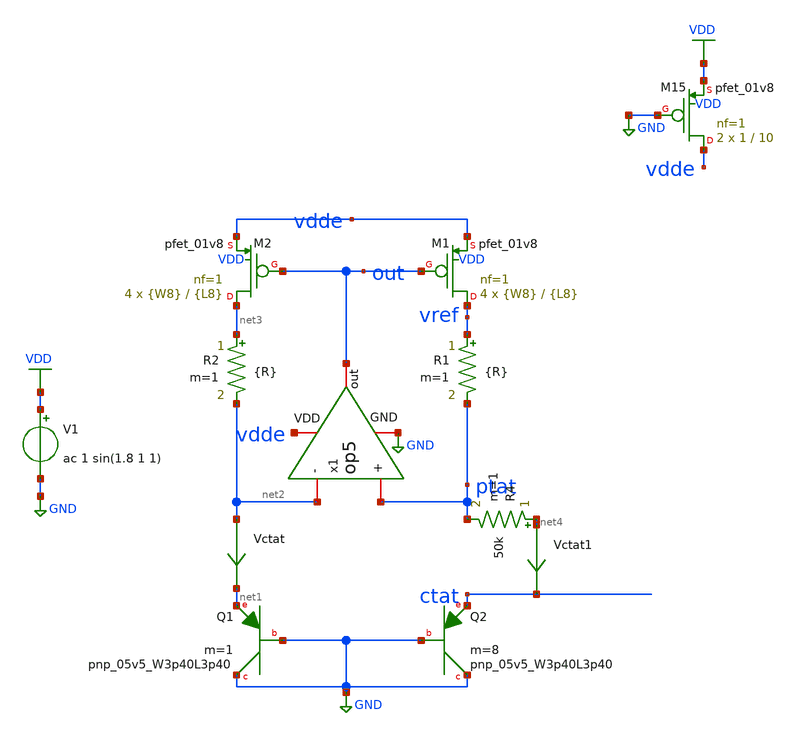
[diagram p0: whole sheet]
** sch_path: xschem/bgr_op5_ideal.sch
**.subckt bgr_op5_ideal
XQ1 GND GND net1 sky130_fd_pr__pnp_05v5_W3p40L3p40 m=1
XQ2 GND GND ctat sky130_fd_pr__pnp_05v5_W3p40L3p40 m=8
Vctat net2 net1 0
.save i(vctat)
V1 VDD GND ac 1 sin(1.8 1 1)
XM1 vref out vdde VDD sky130_fd_pr__pfet_01v8 L={L8} W={W8} nf=1 ad='int((nf+1)/2) * W/nf * 0.29' as='int((nf+2)/2) * W/nf * 0.29'
+ pd='2*int((nf+1)/2) * (W/nf + 0.29)' ps='2*int((nf+2)/2) * (W/nf + 0.29)' nrd='0.29 / W' nrs='0.29 / W'
+ sa=0 sb=0 sd=0 mult=4 m=4
XM2 net3 out vdde VDD sky130_fd_pr__pfet_01v8 L={L8} W={W8} nf=1 ad='int((nf+1)/2) * W/nf * 0.29' as='int((nf+2)/2) * W/nf * 0.29'
+ pd='2*int((nf+1)/2) * (W/nf + 0.29)' ps='2*int((nf+2)/2) * (W/nf + 0.29)' nrd='0.29 / W' nrs='0.29 / W'
+ sa=0 sb=0 sd=0 mult=4 m=4
x1 vdde out net2 ptat GND op5
XM15 vdde GND VDD VDD sky130_fd_pr__pfet_01v8 L=10 W=1 nf=1 ad='int((nf+1)/2) * W/nf * 0.29' as='int((nf+2)/2) * W/nf * 0.29'
+ pd='2*int((nf+1)/2) * (W/nf + 0.29)' ps='2*int((nf+2)/2) * (W/nf + 0.29)' nrd='0.29 / W' nrs='0.29 / W'
+ sa=0 sb=0 sd=0 mult=2 m=2
Vctat1 net4 ctat 0
.save i(vctat1)
R1 vref ptat {R} m=1
R2 net3 net2 {R} m=1
R4 net4 ptat 50k m=1
**** begin user architecture code


.param L8=10
.param W8=1
.param R=492k



** opencircuitdesign pdks install
.lib $::SKYWATER_MODELS/sky130.lib.spice tt




.option savecurrents
.control
save all
op
remzerovec
write bgr_op5_ideal.raw
set appendwrite

dc temp -40 85 1
remzerovec
write bgr_op5_ideal.raw
plot (ptat-ctat)
plot ctat
plot vref
*plot vbgsc vbgtc

********TC********
meas dc temp_avg_vref avg v(vref)
meas dc temp_vref_27 find v(vref) when temp-sweep=27
meas dc temp_pp_vref PP v(vref)
meas dc temp_vref_max max v(vref)
meas dc temp_max_vref when v(vref)='temp_vref_max'
meas dc temp_vref_min min v(vref)
meas dc temp_min_vref when v(vref)='temp_vref_min'
let vref_tc='((temp_pp_vref*1000000)/(125*temp_avg_vref))'
print vref_tc

******PSRR******
ac dec 1000 1 10Meg
write bgr_op5_ideal.raw
remzerovec
plot vdb(vref)
meas ac psrr find vdb(vref) at=1k

****Power****
tran 10ms 5s
write bgr_op5_ideal.raw
set altshow
show >> bgr_op5.lis
remzerovec
meas tran ave_v avg vdd
meas tran ave_i avg i(v1)
let ave_power='ave_v*(-ave_i)
plot vdd vref
*plot -i(v1)
print ave_power

*******LS******
dc v1 0 3.5 0.1
write bgr_op5.raw
remzerovec
plot vdd vref
meas dc vbg_27 find v(vref) at=1.8
meas dc vbgsc_27 find v(vbgsc) at=1.8
meas dc vbgtc_27 find v(vbgtc) at=1.8
meas dc vref_max max v(vref) from=1.62 to=1.98
meas dc vref_min min v(vref) from=1.62 to=1.98
let ls='(vref_max-vref_min)/(1.98-1.62)'
print ls

.endc


**** end user architecture code
**.ends

* expanding   symbol:  op5.sym # of pins=5
** sym_path: xschem/op5.sym
** sch_path: xschem/op5.sch
.subckt op5 VDD out - + GND
*.iopin VDD
*.iopin GND
*.iopin -
*.iopin +
*.iopin out
C2 out net5 2.2p m=1
R2 net5 net1 1k m=1
XM1 bias bias net6 GND sky130_fd_pr__nfet_01v8 L={L5} W={W5} nf=1 ad='int((nf+1)/2) * W/nf * 0.29' as='int((nf+2)/2)
+ * W/nf * 0.29' pd='2*int((nf+1)/2) * (W/nf + 0.29)' ps='2*int((nf+2)/2) * (W/nf + 0.29)' nrd='0.29 /
+ W' nrs='0.29 / W' sa=0 sb=0 sd=0 mult=4 m=4
XM2 net4 bias GND GND sky130_fd_pr__nfet_01v8 L={L5} W={W5} nf=1 ad='int((nf+1)/2) * W/nf * 0.29' as='int((nf+2)/2)
+ * W/nf * 0.29' pd='2*int((nf+1)/2) * (W/nf + 0.29)' ps='2*int((nf+2)/2) * (W/nf + 0.29)' nrd='0.29 /
+ W' nrs='0.29 / W' sa=0 sb=0 sd=0 mult=4 m=4
XM3 net2 - net3 GND sky130_fd_pr__nfet_01v8 L={L4} W={W4} nf=1 ad='int((nf+1)/2) * W/nf * 0.29' as='int((nf+2)/2)
+ * W/nf * 0.29' pd='2*int((nf+1)/2) * (W/nf + 0.29)' ps='2*int((nf+2)/2) * (W/nf + 0.29)' nrd='0.29 /
+ W' nrs='0.29 / W' sa=0 sb=0 sd=0 mult=4 m=4
XM4 net1 + net3 GND sky130_fd_pr__nfet_01v8 L={L4} W={W4} nf=1 ad='int((nf+1)/2) * W/nf * 0.29' as='int((nf+2)/2)
+ * W/nf * 0.29' pd='2*int((nf+1)/2) * (W/nf + 0.29)' ps='2*int((nf+2)/2) * (W/nf + 0.29)' nrd='0.29 /
+ W' nrs='0.29 / W' sa=0 sb=0 sd=0 mult=4 m=4
XM6 bias net4 VDD VDD sky130_fd_pr__pfet_01v8 L={L1} W={W1} nf=1 ad='int((nf+1)/2) * W/nf * 0.29' as='int((nf+2)/2)
+ * W/nf * 0.29' pd='2*int((nf+1)/2) * (W/nf + 0.29)' ps='2*int((nf+2)/2) * (W/nf + 0.29)' nrd='0.29 /
+ W' nrs='0.29 / W' sa=0 sb=0 sd=0 mult=4 m=4
XM7 net4 net4 VDD VDD sky130_fd_pr__pfet_01v8 L={L1} W={W1} nf=1 ad='int((nf+1)/2) * W/nf * 0.29' as='int((nf+2)/2)
+ * W/nf * 0.29' pd='2*int((nf+1)/2) * (W/nf + 0.29)' ps='2*int((nf+2)/2) * (W/nf + 0.29)' nrd='0.29 /
+ W' nrs='0.29 / W' sa=0 sb=0 sd=0 mult=4 m=4
XM8 net1 net2 VDD VDD sky130_fd_pr__pfet_01v8 L={L7} W={W7} nf=1 ad='int((nf+1)/2) * W/nf * 0.29' as='int((nf+2)/2)
+ * W/nf * 0.29' pd='2*int((nf+1)/2) * (W/nf + 0.29)' ps='2*int((nf+2)/2) * (W/nf + 0.29)' nrd='0.29 /
+ W' nrs='0.29 / W' sa=0 sb=0 sd=0 mult=4 m=4
XM9 net2 net2 VDD VDD sky130_fd_pr__pfet_01v8 L={L7} W={W7} nf=1 ad='int((nf+1)/2) * W/nf * 0.29' as='int((nf+2)/2)
+ * W/nf * 0.29' pd='2*int((nf+1)/2) * (W/nf + 0.29)' ps='2*int((nf+2)/2) * (W/nf + 0.29)' nrd='0.29 /
+ W' nrs='0.29 / W' sa=0 sb=0 sd=0 mult=4 m=4
XM5 net3 bias GND GND sky130_fd_pr__nfet_01v8 L={L6} W={W6} nf=1 ad='int((nf+1)/2) * W/nf * 0.29' as='int((nf+2)/2)
+ * W/nf * 0.29' pd='2*int((nf+1)/2) * (W/nf + 0.29)' ps='2*int((nf+2)/2) * (W/nf + 0.29)' nrd='0.29 /
+ W' nrs='0.29 / W' sa=0 sb=0 sd=0 mult=4 m=4
XM10 out net1 VDD VDD sky130_fd_pr__pfet_01v8 L={L2} W={W2} nf=1 ad='int((nf+1)/2) * W/nf * 0.29' as='int((nf+2)/2)
+ * W/nf * 0.29' pd='2*int((nf+1)/2) * (W/nf + 0.29)' ps='2*int((nf+2)/2) * (W/nf + 0.29)' nrd='0.29 /
+ W' nrs='0.29 / W' sa=0 sb=0 sd=0 mult=4 m=4
XM11 out bias GND GND sky130_fd_pr__nfet_01v8 L={L3} W={W3} nf=1 ad='int((nf+1)/2) * W/nf * 0.29' as='int((nf+2)/2)
+ * W/nf * 0.29' pd='2*int((nf+1)/2) * (W/nf + 0.29)' ps='2*int((nf+2)/2) * (W/nf + 0.29)' nrd='0.29 /
+ W' nrs='0.29 / W' sa=0 sb=0 sd=0 mult=4 m=4
R3 net6 GND 5k m=1
**** begin user architecture code


**************
*PMOS cms
.param L1=2.7
.param W1=1.25

**************
*NMOS cms
.param L5=2
.param W5=3.5

**************
*PMOS current differential
.param L7=2.7
.param W7=1.25

**************
*differential Pair
.param L4=2.7
.param W4=1.25

**************
*NMOS current control
.param L6=2
.param W6=3.5

**************
*Second Stage
.param L2=2
.param W2=3.5

**************
*NMOS current second stage
.param L3=2
.param W3=3.5


**** end user architecture code
.ends

.GLOBAL GND
.GLOBAL VDD
.end
